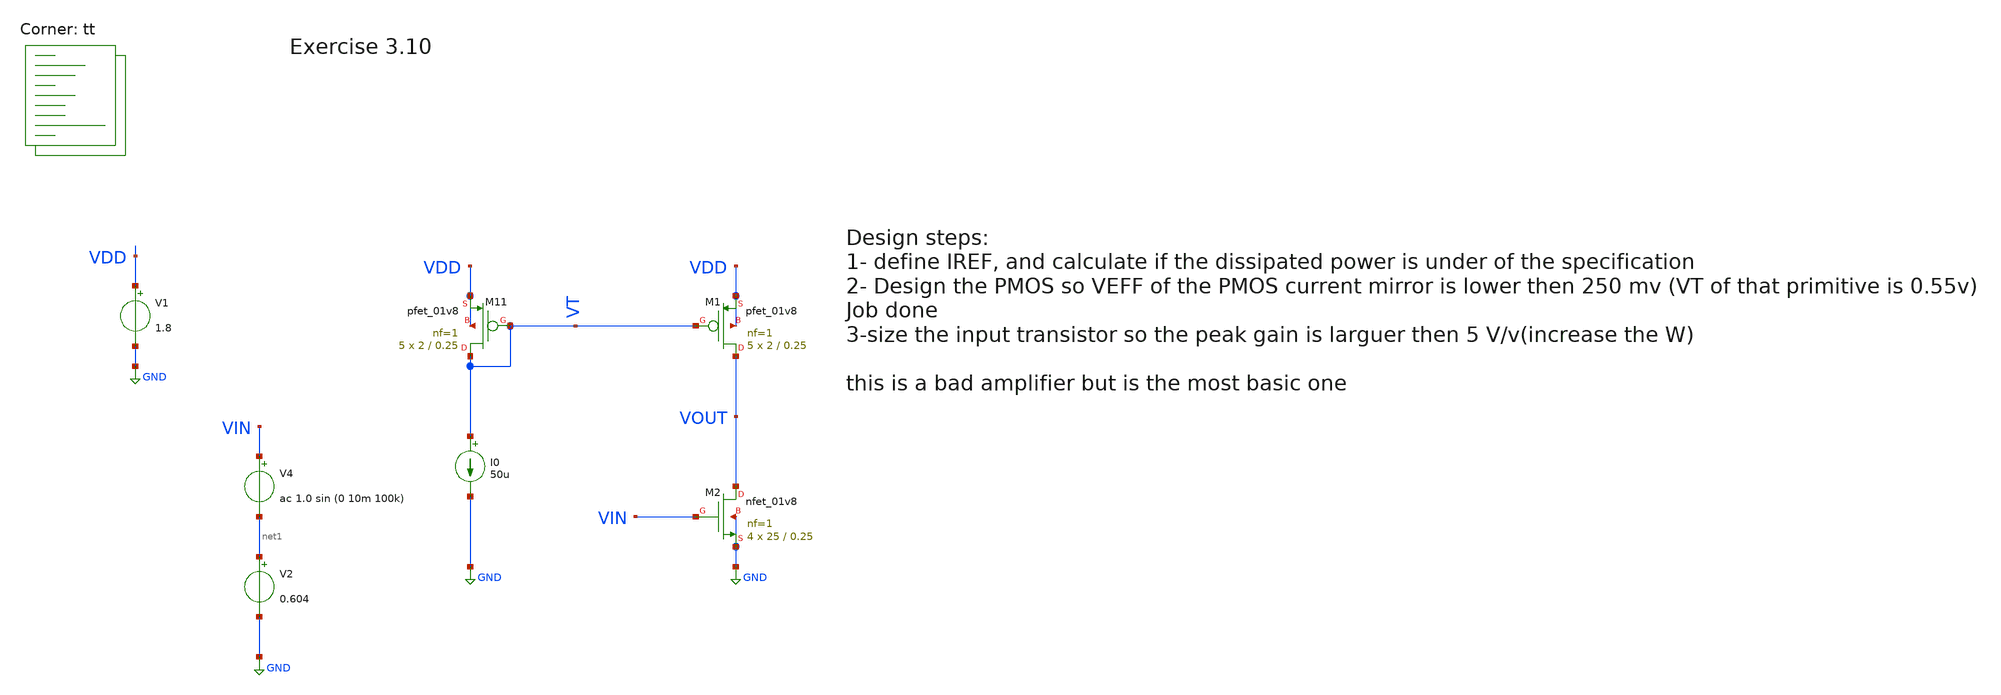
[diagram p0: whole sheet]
** sch_path: Analog_integrated_circuit_Design/chapter3/10/10.sch
**.subckt 10
V1 VDD GND 1.8
XM11 VT VT VDD VDD sky130_fd_pr__pfet_01v8 L=0.25 W=2 nf=1 ad='int((nf+1)/2) * W/nf * 0.29' as='int((nf+2)/2) * W/nf * 0.29'
+ pd='2*int((nf+1)/2) * (W/nf + 0.29)' ps='2*int((nf+2)/2) * (W/nf + 0.29)' nrd='0.29 / W' nrs='0.29 / W'
+ sa=0 sb=0 sd=0 mult=5 m=5
I0 VT GND 50u
XM1 VOUT VT VDD VDD sky130_fd_pr__pfet_01v8 L=0.25 W=2 nf=1 ad='int((nf+1)/2) * W/nf * 0.29' as='int((nf+2)/2) * W/nf * 0.29'
+ pd='2*int((nf+1)/2) * (W/nf + 0.29)' ps='2*int((nf+2)/2) * (W/nf + 0.29)' nrd='0.29 / W' nrs='0.29 / W'
+ sa=0 sb=0 sd=0 mult=5 m=5
XM2 VOUT VIN GND GND sky130_fd_pr__nfet_01v8 L=0.25 W=25 nf=1 ad='int((1 + 1)/2) * 25 / 1 * 0.29' as='int((1 + 2)/2) * 25 / 1 * 0.29'
+ pd='2*int((1 + 1)/2) * (25 / 1 + 0.29)' ps='2*int((1 + 2)/2) * (25 / 1 + 0.29)' nrd='0.29 / 25 ' nrs='0.29 / 25 '
+ sa=0 sb=0 sd=0 mult=4 m=4
V2 net1 GND 0.604
V4 VIN net1 ac 1.0 sin (0 10m 100k)
**** begin user architecture code
.lib $::SKYWATER_MODELS/sky130.lib.spice tt

**************************************************************
**************************************************************
**************************************************************
**************************************************************
**************************************************************
*LIBs*********************************************************
**************************************************************
**************************************************************
**************************************************************
**************************************************************
**************************************************************
*.lib $::SKYWATER_MODELS/sky130.lib.spice tt
* chose the corners in the corner file
* tt_mm for mismatch
* ss ff sf fs standart corners
* ll hh lh hl capacitor and resistors corners
* mc for total process variation including corners
**************************************************************
**************************************************************
**************************************************************
**************************************************************
**************************************************************
*Corners/montecarlo options***********************************
**************************************************************
**************************************************************
**************************************************************
**************************************************************
**************************************************************
.TEMP 27
**************************************************************
**************************************************************
**************************************************************
**************************************************************
*SIMULATION and Plots*****************************************
**************************************************************
**************************************************************
**************************************************************
**************************************************************
.control
save all
dc V2 0 1.8 0.001
*dc simulation
plot deriv(V(Vout)) v(VOUT)
plot v(VT)
ac dec 20 1 50G
plot db(v(VOUT))
.endc

**** end user architecture code
**.ends
.GLOBAL GND
.end
